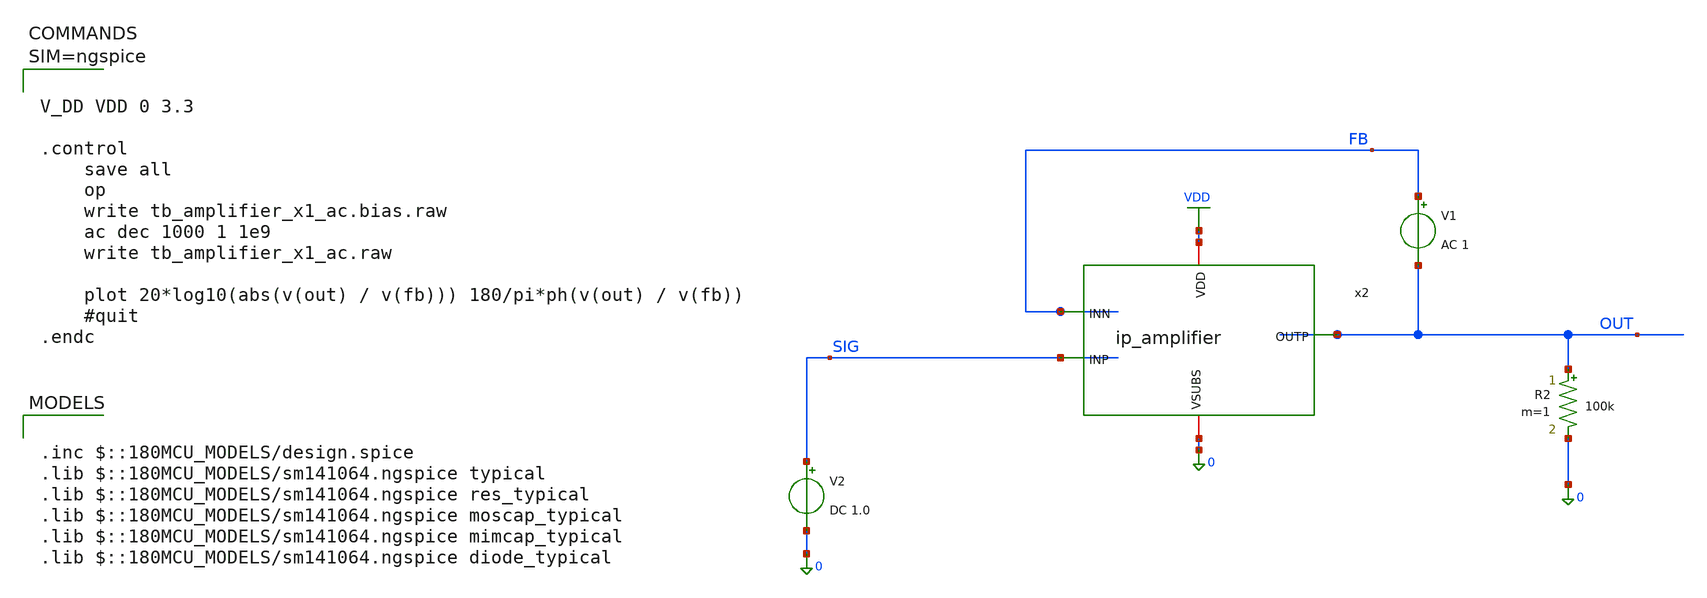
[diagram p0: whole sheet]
** sch_path: xschem/tb_amplifier_x1_ac.sch
**.subckt tb_amplifier_x1_ac
V2 SIG 0 DC 1.0
x2 VDD OUT SIG FB 0 ip_amplifier
R2 OUT 0 100k m=1
V1 FB OUT AC 1
**** begin user architecture code

.inc $::180MCU_MODELS/design.spice
.lib $::180MCU_MODELS/sm141064.ngspice typical
.lib $::180MCU_MODELS/sm141064.ngspice res_typical
.lib $::180MCU_MODELS/sm141064.ngspice moscap_typical
.lib $::180MCU_MODELS/sm141064.ngspice mimcap_typical
.lib $::180MCU_MODELS/sm141064.ngspice diode_typical




V_DD VDD 0 3.3

.control
	save all
	op
	write tb_amplifier_x1_ac.bias.raw
	ac dec 1000 1 1e9
	write tb_amplifier_x1_ac.raw

	plot 20*log10(abs(v(out) / v(fb))) 180/pi*ph(v(out) / v(fb))
	#quit
.endc



**** end user architecture code
**.ends
.GLOBAL VDD
.end
